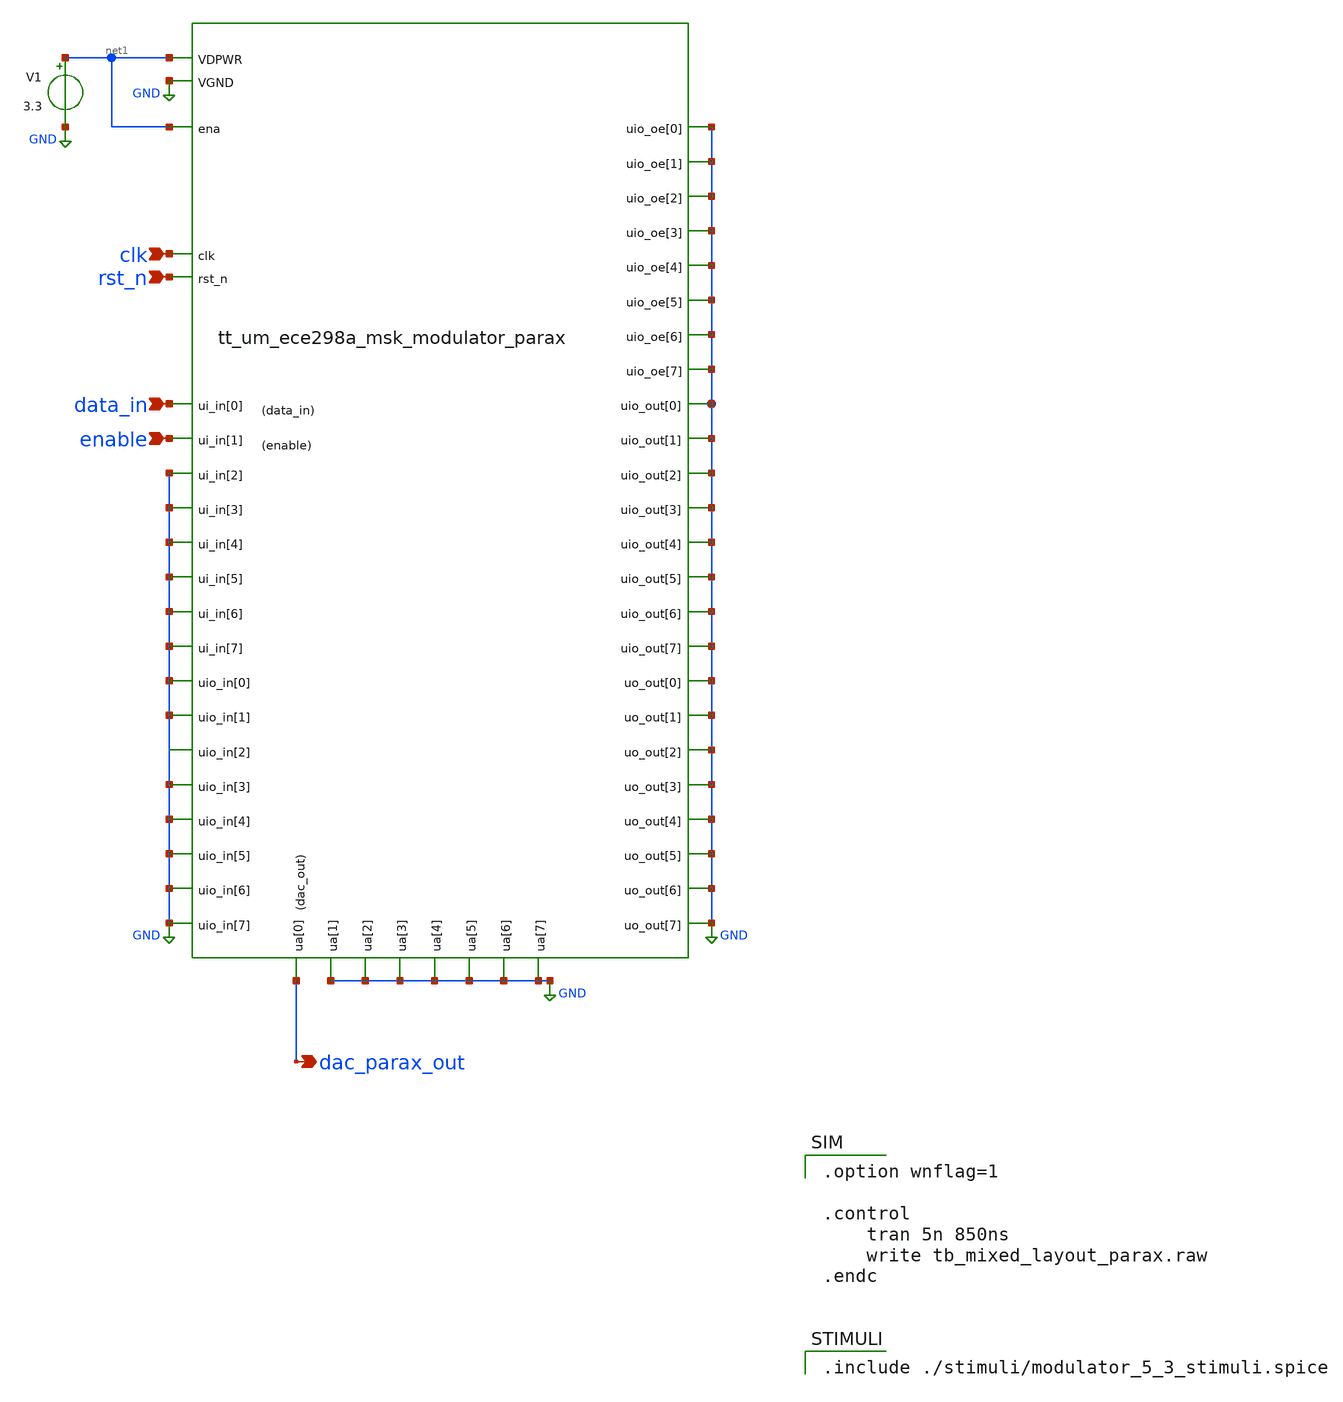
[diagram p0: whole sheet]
** sch_path: xschem/tb_mixed_layout_parax.sch
**.subckt tb_mixed_layout_parax data_in enable clk rst_n dac_parax_out
*.ipin data_in
*.ipin enable
*.ipin clk
*.ipin rst_n
*.opin dac_parax_out
V1 net1 GND 3.3
x1 clk net1 rst_n dac_parax_out GND GND GND GND GND GND GND data_in enable GND GND GND GND GND GND
+ GND GND GND GND GND GND GND GND GND GND GND GND GND GND GND GND GND GND GND GND GND GND GND GND GND GND
+ GND GND GND GND GND GND net1 tt_um_ece298a_msk_modulator_parax
**** begin user architecture code

.option wnflag=1

.control
    tran 5n 850ns
    write tb_mixed_layout_parax.raw
.endc



.include ./stimuli/modulator_5_3_stimuli.spice


.include /usr/local/share/pdk/gf180mcuD/libs.tech/ngspice/design.ngspice
.lib /usr/local/share/pdk/gf180mcuD/libs.tech/ngspice/sm141064.ngspice typical
.lib /usr/local/share/pdk/gf180mcuD/libs.tech/ngspice/sm141064.ngspice res_typical

**** end user architecture code
**.ends

* expanding   symbol:  tt_um_ece298a_msk_modulator_parax.sym # of pins=52
** sym_path: xschem/tt_um_ece298a_msk_modulator_parax.sym
.include ../../mag/spice/tt_um_ece298a_msk_modulator_parax.spice
.GLOBAL GND
.end
